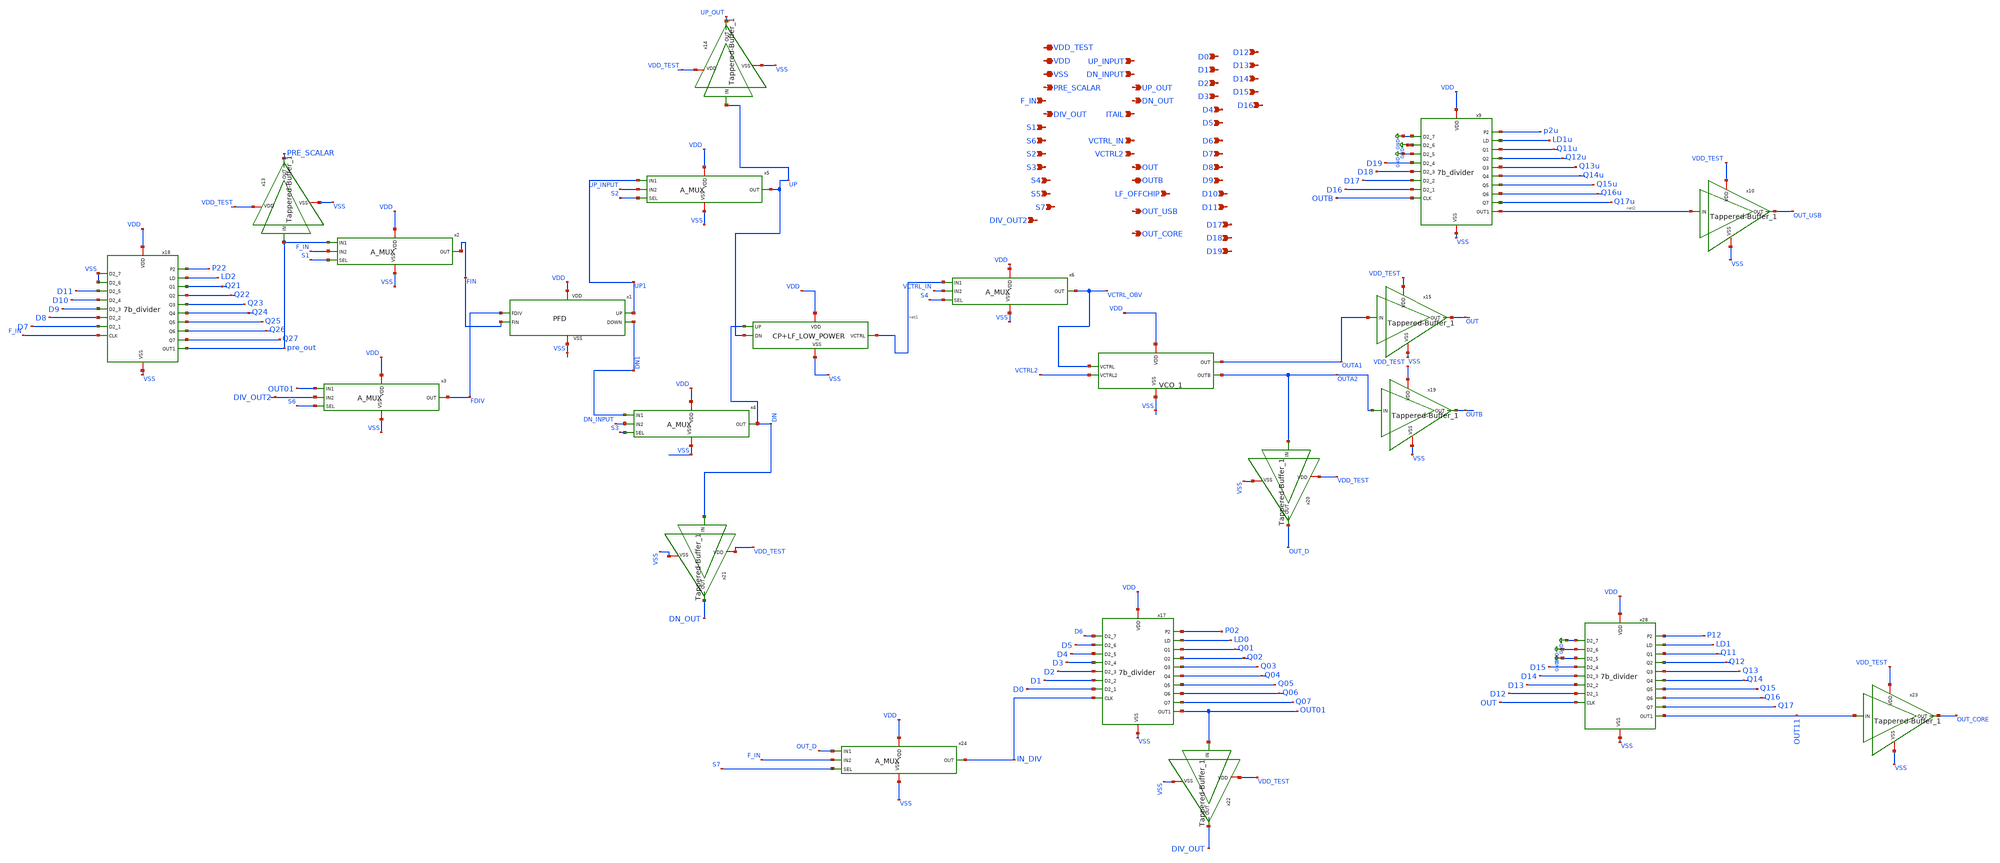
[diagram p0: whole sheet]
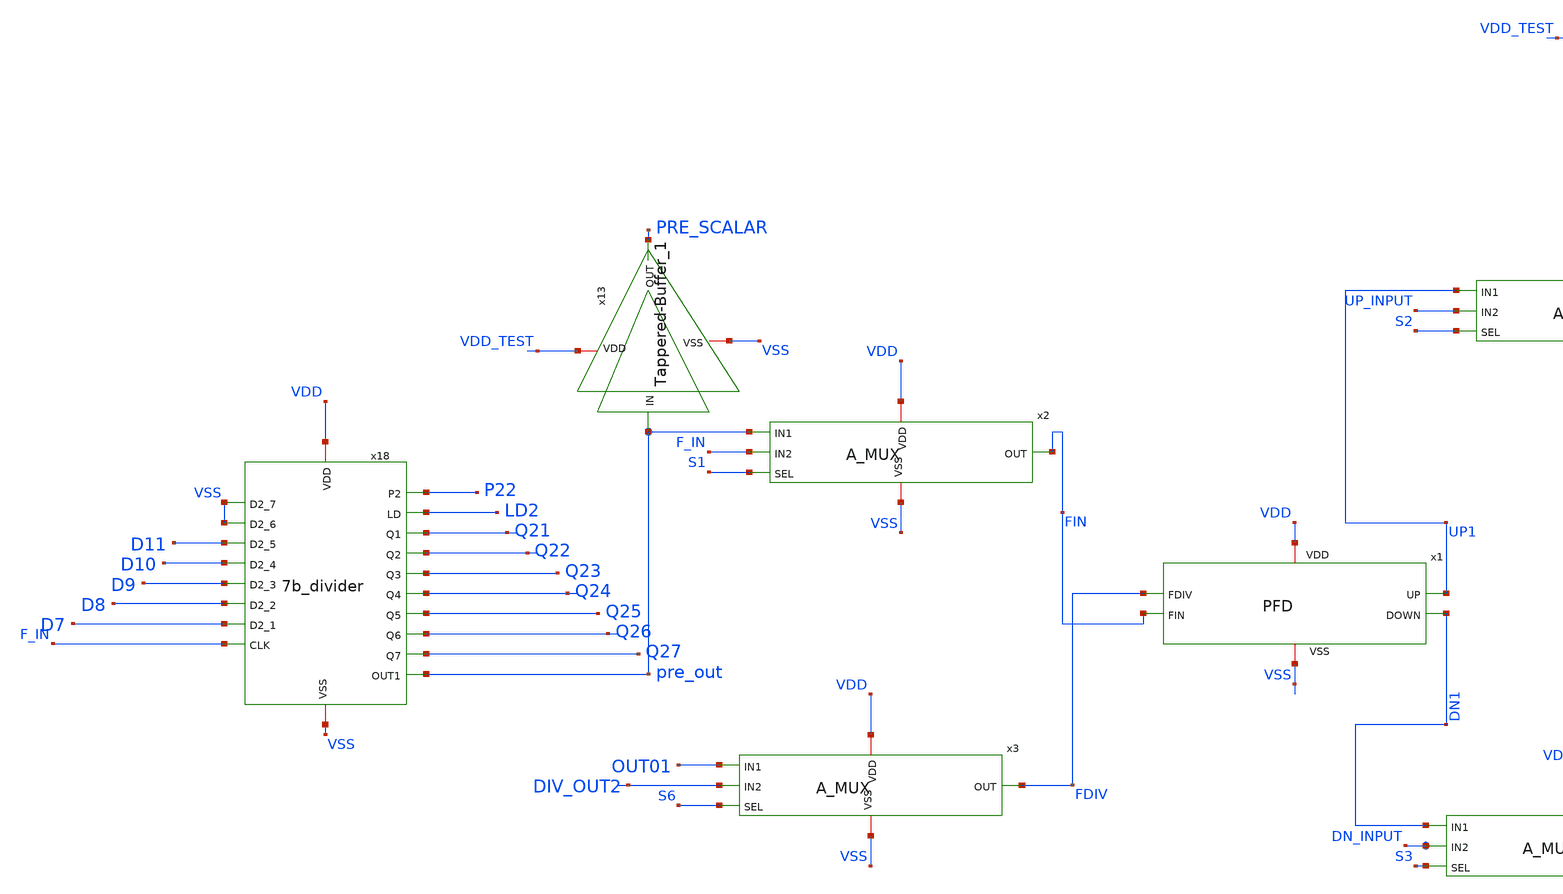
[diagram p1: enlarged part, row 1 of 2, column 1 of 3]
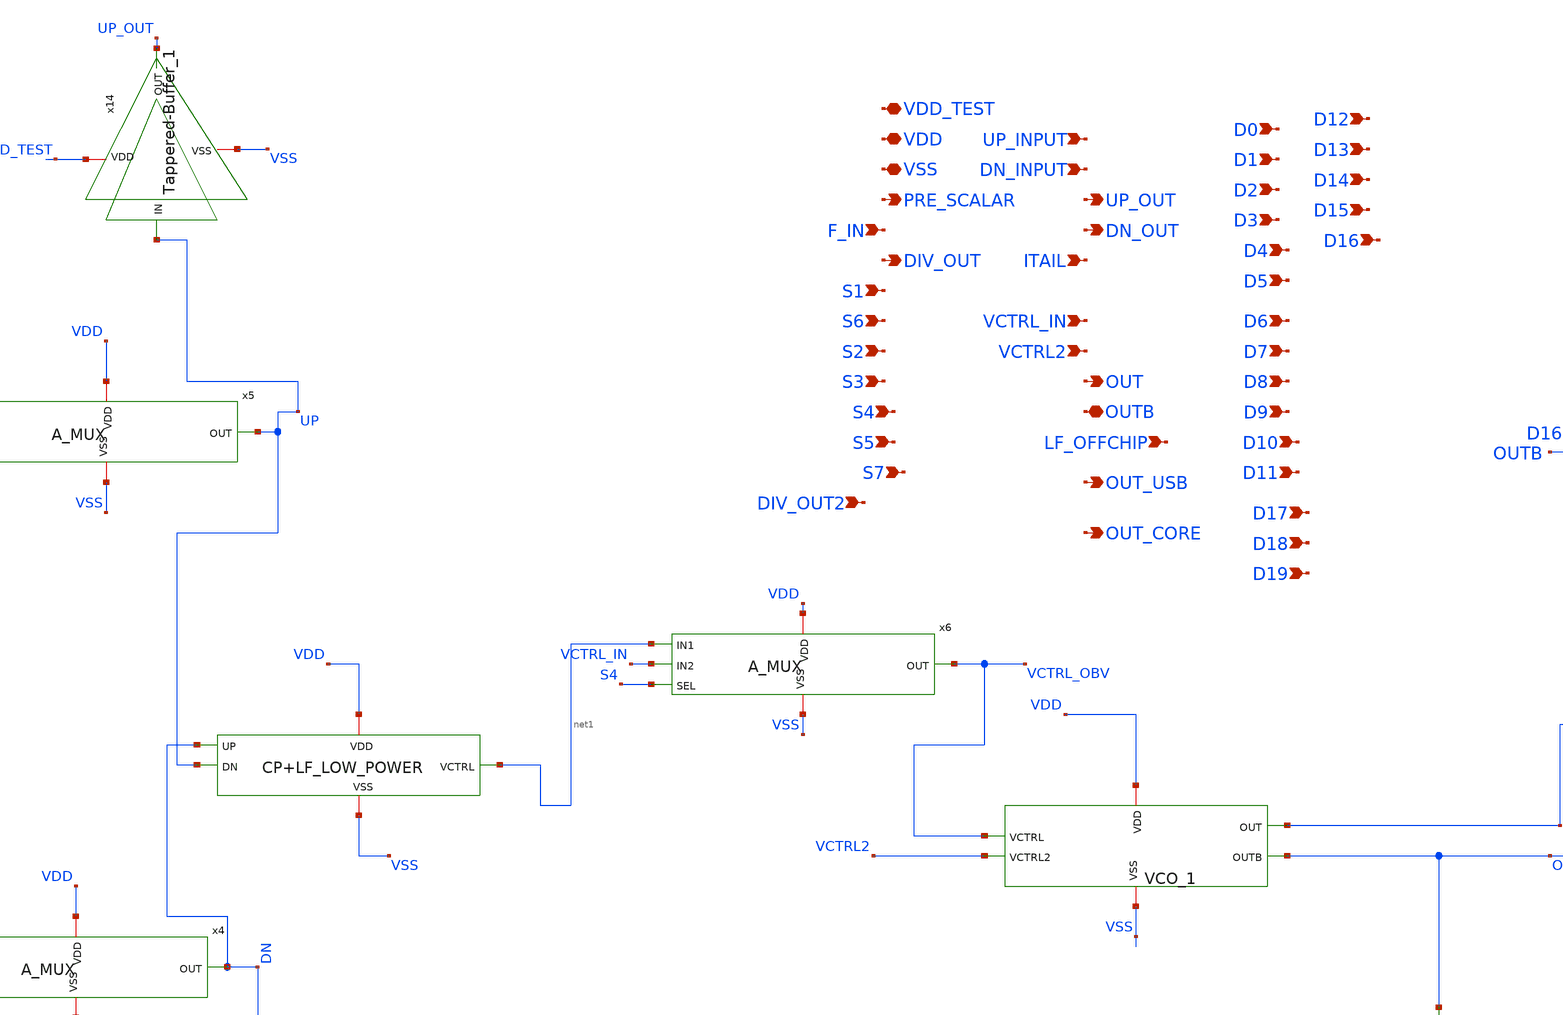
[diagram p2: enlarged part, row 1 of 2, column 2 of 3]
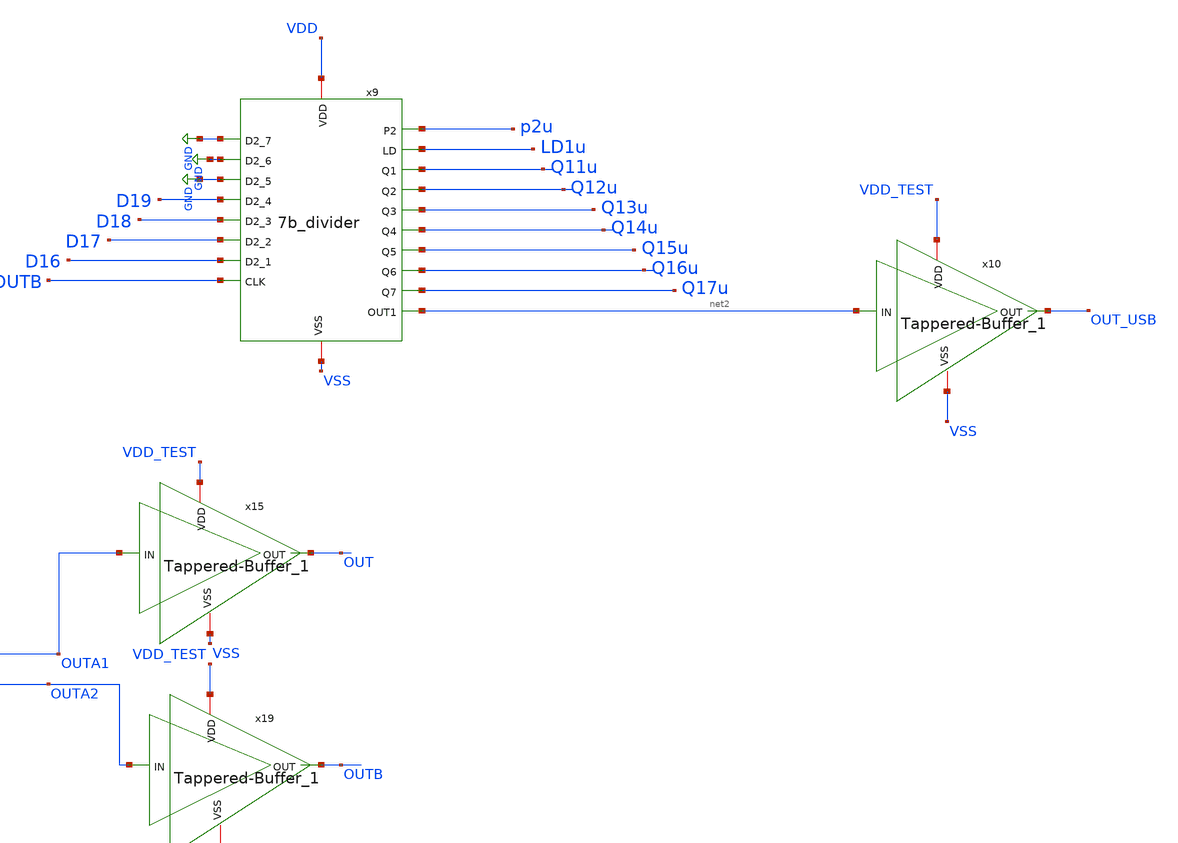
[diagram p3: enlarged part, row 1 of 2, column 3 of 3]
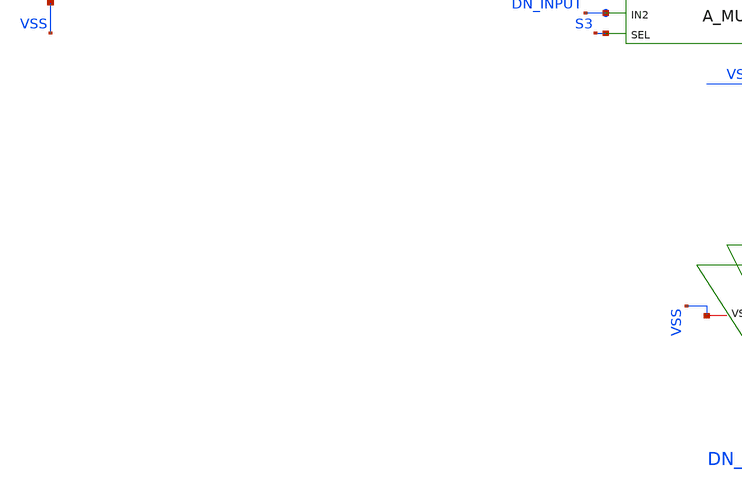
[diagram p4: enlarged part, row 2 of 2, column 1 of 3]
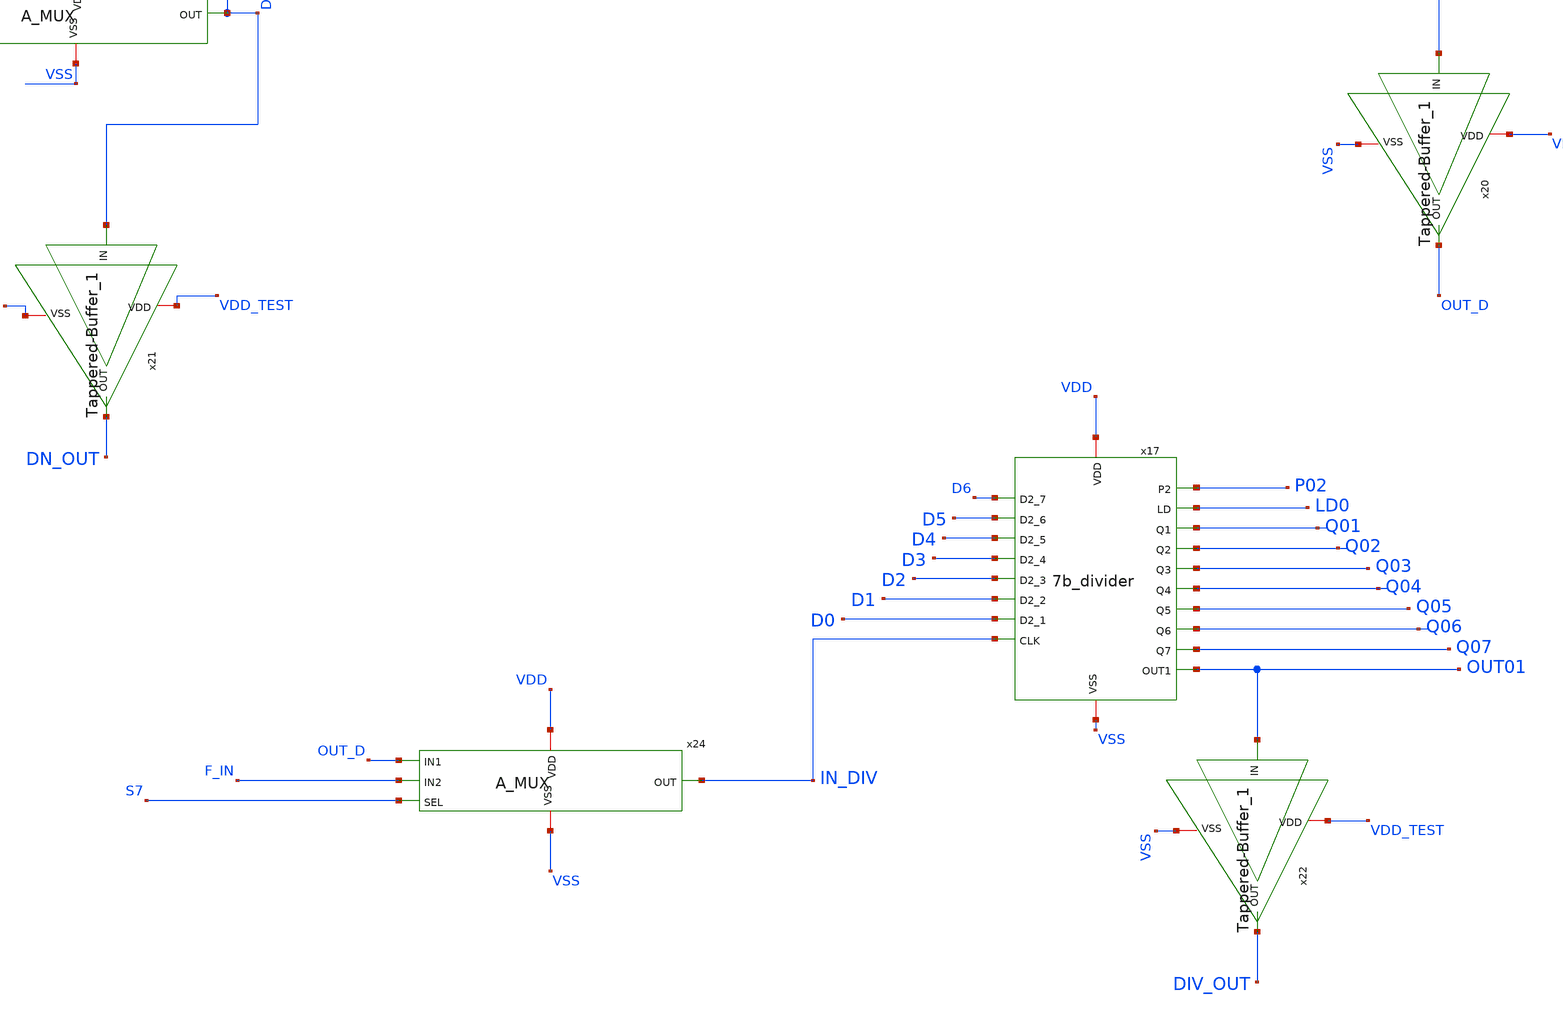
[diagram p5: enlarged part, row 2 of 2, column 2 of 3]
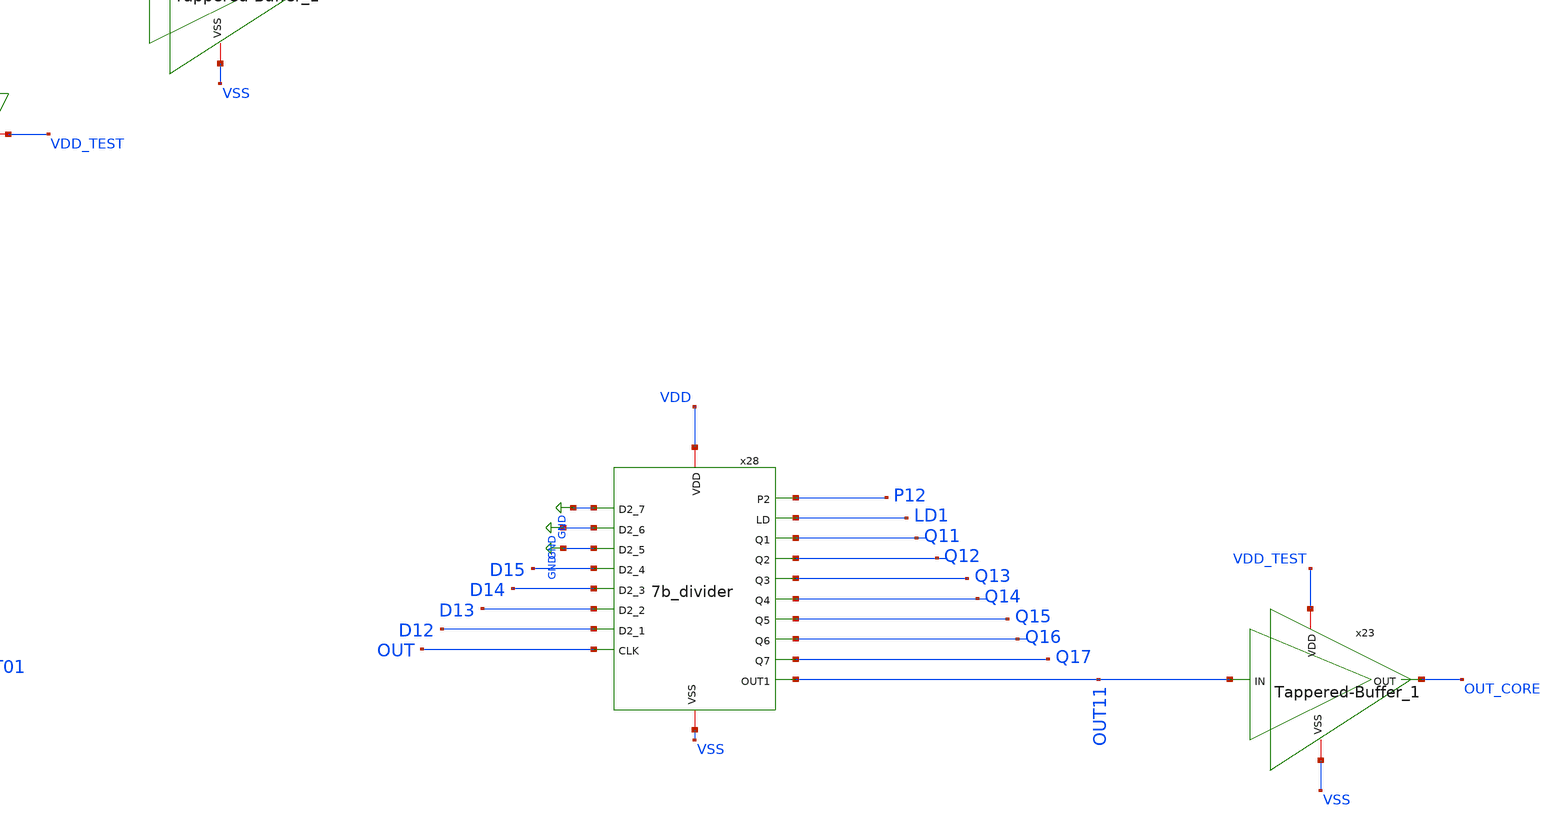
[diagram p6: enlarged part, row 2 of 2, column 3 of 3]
** sch_path: Xschem/PLL_TOP_Schematics/PLL_TOP_LOW_POWER.sch
**.subckt PLL_TOP_LOW_POWER UP_INPUT DN_INPUT UP_OUT DN_OUT ITAIL VCTRL2 OUT OUTB VDD VSS PRE_SCALAR
*+ F_IN DIV_OUT S1 S6 S2 S3 VCTRL_IN S4 S5 LF_OFFCHIP D0 D1 D2 D3 D4 D5 D6 D7 D8 D9 D10 D11 D12 D13 D14 D15
*+ D16 OUT_USB S7 VDD_TEST DIV_OUT2 D17 D18 D19 OUT_CORE
*.ipin UP_INPUT
*.ipin DN_INPUT
*.opin UP_OUT
*.opin DN_OUT
*.ipin ITAIL
*.ipin VCTRL2
*.opin OUT
*.iopin OUTB
*.iopin VDD
*.iopin VSS
*.opin PRE_SCALAR
*.ipin F_IN
*.opin DIV_OUT
*.ipin S1
*.ipin S6
*.ipin S2
*.ipin S3
*.ipin VCTRL_IN
*.ipin S4
*.ipin S5
*.ipin LF_OFFCHIP
*.ipin D0
*.ipin D1
*.ipin D2
*.ipin D3
*.ipin D4
*.ipin D5
*.ipin D6
*.ipin D7
*.ipin D8
*.ipin D9
*.ipin D10
*.ipin D11
*.ipin D12
*.ipin D13
*.ipin D14
*.ipin D15
*.ipin D16
*.opin OUT_USB
*.ipin S7
*.iopin VDD_TEST
*.ipin DIV_OUT2
*.ipin D17
*.ipin D18
*.ipin D19
*.opin OUT_CORE
x18 VDD LD2 VSS Q21 VSS Q22 D11 D10 Q23 Q24 D9 D8 Q25 D7 Q26 Q27 F_IN VSS pre_out P22 7b_divider
x17 VDD LD0 D6 Q01 D5 Q02 D4 D3 Q03 Q04 D2 D1 Q05 D0 Q06 Q07 IN_DIV VSS OUT01 P02 7b_divider
x28 VDD LD1 GND Q11 GND Q12 GND D15 Q13 Q14 D14 D13 Q15 D12 Q16 Q17 OUT VSS OUT11 P12 7b_divider
x13 VSS VDD_TEST PRE_SCALAR pre_out Tappered-Buffer_1
x14 VSS VDD_TEST UP_OUT UP Tappered-Buffer_1
x15 VSS VDD_TEST OUT OUTA1 Tappered-Buffer_1
x19 VSS VDD_TEST OUTB OUTA2 Tappered-Buffer_1
x20 VSS VDD_TEST OUT_D OUTA2 Tappered-Buffer_1
x21 VSS VDD_TEST DN_OUT DN Tappered-Buffer_1
x22 VSS VDD_TEST DIV_OUT OUT01 Tappered-Buffer_1
x23 VSS VDD_TEST OUT_CORE OUT11 Tappered-Buffer_1
x2 VDD VSS pre_out F_IN S1 FIN A_MUX
x3 VDD VSS OUT01 DIV_OUT2 S6 FDIV A_MUX
x4 VDD VSS DN1 DN_INPUT S3 DN A_MUX
x5 VDD VSS UP1 UP_INPUT S2 UP A_MUX
x6 VDD VSS net1 VCTRL_IN S4 VCTRL_OBV A_MUX
x7 VDD VSS VCTRL_OBV VCTRL2 OUTA1 OUTA2 VCO_1
x24 VDD VSS OUT_D F_IN S7 IN_DIV A_MUX
x9 VDD LD1u GND Q11u GND Q12u GND D19 Q13u Q14u D18 D17 Q15u D16 Q16u Q17u OUTB VSS net2 p2u
+ 7b_divider
x10 VSS VDD_TEST OUT_USB net2 Tappered-Buffer_1
x8 VDD VSS DN UP net1 CP+LF_LOW_POWER
x1 VDD VSS FDIV FIN UP1 DN1 PFD
**.ends
.GLOBAL GND
.end
